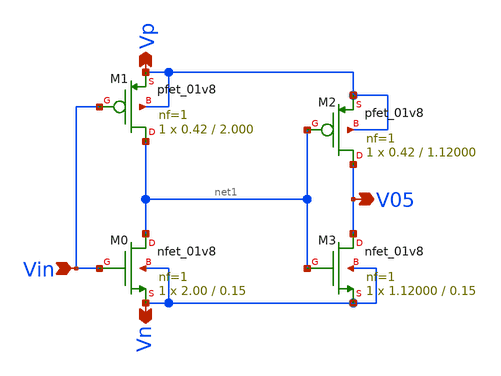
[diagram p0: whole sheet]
** sch_path: xschem/Vth_sch/Symbol/th05_backup.sch
**.subckt th05_backup Vn Vp Vin V05
*.opin Vn
*.opin Vp
*.ipin Vin
*.opin V05
XM2 V05 net1 Vp Vp sky130_fd_pr__pfet_01v8 L=1.12000 W=0.42 nf=1 ad='int((nf+1)/2) * W/nf * 0.29' as='int((nf+2)/2) * W/nf * 0.29'
+ pd='2*int((nf+1)/2) * (W/nf + 0.29)' ps='2*int((nf+2)/2) * (W/nf + 0.29)' nrd='0.29 / W' nrs='0.29 / W'
+ sa=0 sb=0 sd=0 mult=1 m=1
XM3 V05 net1 Vn Vn sky130_fd_pr__nfet_01v8 L=0.15 W=1.12000 nf=1 ad='int((nf+1)/2) * W/nf * 0.29' as='int((nf+2)/2) * W/nf * 0.29'
+ pd='2*int((nf+1)/2) * (W/nf + 0.29)' ps='2*int((nf+2)/2) * (W/nf + 0.29)' nrd='0.29 / W' nrs='0.29 / W'
+ sa=0 sb=0 sd=0 mult=1 m=1
XM1 net1 Vin Vp Vp sky130_fd_pr__pfet_01v8 L=2.000 W=0.42 nf=1 ad='int((nf+1)/2) * W/nf * 0.29' as='int((nf+2)/2) * W/nf * 0.29'
+ pd='2*int((nf+1)/2) * (W/nf + 0.29)' ps='2*int((nf+2)/2) * (W/nf + 0.29)' nrd='0.29 / W' nrs='0.29 / W'
+ sa=0 sb=0 sd=0 mult=1 m=1
XM0 net1 Vin Vn Vn sky130_fd_pr__nfet_01v8 L=0.15 W=2.00 nf=1 ad='int((nf+1)/2) * W/nf * 0.29' as='int((nf+2)/2) * W/nf * 0.29'
+ pd='2*int((nf+1)/2) * (W/nf + 0.29)' ps='2*int((nf+2)/2) * (W/nf + 0.29)' nrd='0.29 / W' nrs='0.29 / W'
+ sa=0 sb=0 sd=0 mult=1 m=1
**.ends
.end
